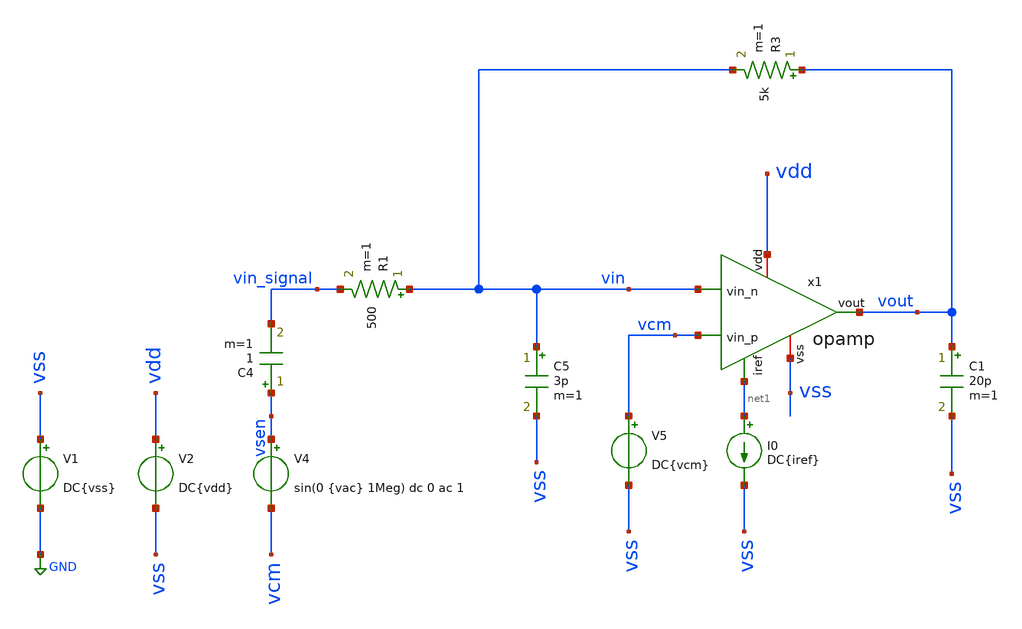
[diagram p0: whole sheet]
** sch_path: tb_opamp_closeloop.sch
**.subckt tb_opamp_closeloop
V1 vss GND DC{vss}
V2 vdd vss DC{vdd}
V4 vsen vcm sin(0 {vac} 1Meg) dc 0 ac 1
C4 vsen vin_signal 1 m=1
I0 net1 vss DC{iref}
R1 vin vin_signal 500 m=1
R3 vout vin 5k m=1
C5 vin vss 3p m=1
C1 vout vss 20p m=1
V5 vcm vss DC{vcm}
x1 vdd net1 vin vcm vout vss opamp
**** begin user architecture code




* Circuit Parameters
.param iref = 100u
.param vdd  = 1.8
.param vss  = 0.0
.param vcm  = vdd/2
.param vac  = 60m

.param mul8 = 2
.param mul5 = 20
.param mul7 = 150
.param w857 = 70
.param l857 = 7

.param l34  = 3
.param w34  = 60
.param mul34 = 2

.param mpar = 333
.param lpar = 0.5
.param wpar = 10

.param mul6 = 90
.param l6   = 0.15
.param w6   = 25

.param mul9 = 1
.param l9   = 0.15
.param w9   = 10

.param res_1 = 333
.param cap_1 = 5p

.options TEMP = 65

* Include Models
.lib ~/skywater/skywater-pdk/libraries/sky130_fd_pr_ngspice/latest/models/corners/sky130.lib TT

* OP Parameters & Singals to save
.save all  @M.X1.XM1.msky130_fd_pr__pfet_01v8_lvt[id] @M.X1.XM1.msky130_fd_pr__pfet_01v8_lvt[vth] @M.X1.XM1.msky130_fd_pr__pfet_01v8_lvt[vgs] @M.X1.XM1.msky130_fd_pr__pfet_01v8_lvt[vds] @M.X1.XM1.msky130_fd_pr__pfet_01v8_lvt[vdsat] @M.X1.XM1.msky130_fd_pr__pfet_01v8_lvt[gm] @M.X1.XM1.msky130_fd_pr__pfet_01v8_lvt[gds]  @M.X1.XM2.msky130_fd_pr__pfet_01v8_lvt[id] @M.X1.XM2.msky130_fd_pr__pfet_01v8_lvt[vth] @M.X1.XM2.msky130_fd_pr__pfet_01v8_lvt[vgs] @M.X1.XM2.msky130_fd_pr__pfet_01v8_lvt[vds] @M.X1.XM2.msky130_fd_pr__pfet_01v8_lvt[vdsat] @M.X1.XM2.msky130_fd_pr__pfet_01v8_lvt[gm] @M.X1.XM2.msky130_fd_pr__pfet_01v8_lvt[gds]  @M.X1.XM3.msky130_fd_pr__nfet_01v8[id] @M.X1.XM3.msky130_fd_pr__nfet_01v8[vth] @M.X1.XM3.msky130_fd_pr__nfet_01v8[vgs] @M.X1.XM3.msky130_fd_pr__nfet_01v8[vds] @M.X1.XM3.msky130_fd_pr__nfet_01v8[vdsat] @M.X1.XM3.msky130_fd_pr__nfet_01v8[gm] @M.X1.XM3.msky130_fd_pr__nfet_01v8[gds]  @M.X1.XM4.msky130_fd_pr__nfet_01v8[id] @M.X1.XM4.msky130_fd_pr__nfet_01v8[vth] @M.X1.XM4.msky130_fd_pr__nfet_01v8[vgs] @M.X1.XM4.msky130_fd_pr__nfet_01v8[vds] @M.X1.XM4.msky130_fd_pr__nfet_01v8[vdsat] @M.X1.XM4.msky130_fd_pr__nfet_01v8[gm] @M.X1.XM4.msky130_fd_pr__nfet_01v8[gds]  @M.X1.XM5.msky130_fd_pr__pfet_01v8[id] @M.X1.XM5.msky130_fd_pr__pfet_01v8[vth] @M.X1.XM5.msky130_fd_pr__pfet_01v8[vgs] @M.X1.XM5.msky130_fd_pr__pfet_01v8[vds] @M.X1.XM5.msky130_fd_pr__pfet_01v8[vdsat] @M.X1.XM5.msky130_fd_pr__pfet_01v8[gm] @M.X1.XM5.msky130_fd_pr__pfet_01v8[gds]  @M.X1.XM6.msky130_fd_pr__nfet_01v8[id] @M.X1.XM6.msky130_fd_pr__nfet_01v8[vth] @M.X1.XM6.msky130_fd_pr__nfet_01v8[vgs] @M.X1.XM6.msky130_fd_pr__nfet_01v8[vds] @M.X1.XM6.msky130_fd_pr__nfet_01v8[vdsat] @M.X1.XM6.msky130_fd_pr__nfet_01v8[gm] @M.X1.XM6.msky130_fd_pr__nfet_01v8[gds]  @M.X1.XM7.msky130_fd_pr__pfet_01v8[id] @M.X1.XM7.msky130_fd_pr__pfet_01v8[vth] @M.X1.XM7.msky130_fd_pr__pfet_01v8[vgs] @M.X1.XM7.msky130_fd_pr__pfet_01v8[vds] @M.X1.XM7.msky130_fd_pr__pfet_01v8[vdsat] @M.X1.XM7.msky130_fd_pr__pfet_01v8[gm] @M.X1.XM7.msky130_fd_pr__pfet_01v8[gds]  @M.X1.XM8.msky130_fd_pr__pfet_01v8[id] @M.X1.XM8.msky130_fd_pr__pfet_01v8[vth] @M.X1.XM8.msky130_fd_pr__pfet_01v8[vgs] @M.X1.XM8.msky130_fd_pr__pfet_01v8[vds] @M.X1.XM8.msky130_fd_pr__pfet_01v8[vdsat] @M.X1.XM8.msky130_fd_pr__pfet_01v8[gm] @M.X1.XM8.msky130_fd_pr__pfet_01v8[gds]  @M.X1.XM9.msky130_fd_pr__nfet_01v8[id] @M.X1.XM9.msky130_fd_pr__nfet_01v8[vth] @M.X1.XM9.msky130_fd_pr__nfet_01v8[vgs] @M.X1.XM9.msky130_fd_pr__nfet_01v8[vds] @M.X1.XM9.msky130_fd_pr__nfet_01v8[vdsat] @M.X1.XM9.msky130_fd_pr__nfet_01v8[gm] @M.X1.XM9.msky130_fd_pr__nfet_01v8[gds]  @M.X1.XM6.msky130_fd_pr__nfet_01v8[cgg] @M.X1.XM1.msky130_fd_pr__nfet_01v8[vdsat] @M.X1.XM2.msky130_fd_pr__nfet_01v8[vdsat] @M.X1.XM3.msky130_fd_pr__nfet_01v8[vdsat] @M.X1.XM4.msky130_fd_pr__nfet_01v8[vdsat] @M.X1.XM5.msky130_fd_pr__nfet_01v8[vdsat] @M.X1.XM6.msky130_fd_pr__nfet_01v8[vdsat] @M.X1.XM7.msky130_fd_pr__nfet_01v8[vdsat] @M.X1.XM8.msky130_fd_pr__nfet_01v8[vdsat] @M.X1.XM9.msky130_fd_pr__nfet_01v8[vdsat]
*
*Simulation
.control
  set color1 = purple
  set color0 = white
  ac dec 100 1k 10G
  setplot ac1
  meas ac GBW when vdb(vout)=0
  meas ac DCG find vdb(vout) at=1k
  plot vdb(vout) {vp(vout)*180/PI}

  reset
  tran 0.01u 11u
  setplot tran1
  plot v(vsen) v(vout)

  *reset
  *noise v(vout) V4 dec 100 1k 10G 1
  *setplot noise1
  *plot inoise_spectrum onoise_spectrum
  *plot onoise_spectrum onoise_spectrum
  *setplot noise2
  *print inoise_total
  *print onoise_total
  *print onoise_total.m.x1.xm1.msky130_fd_pr__pfet_01v8_lvt.1overf
  *print onoise_total.m.x1.xm1.msky130_fd_pr__pfet_01v8_lvt.id
  *print onoise_total.m.x1.xm2.msky130_fd_pr__pfet_01v8_lvt.1overf
  *print onoise_total.m.x1.xm2.msky130_fd_pr__pfet_01v8_lvt.id
  *print onoise_total.m.x1.xm3.msky130_fd_pr__nfet_01v8.1overf
  *print onoise_total.m.x1.xm3.msky130_fd_pr__nfet_01v8.id
  *print onoise_total.m.x1.xm4.msky130_fd_pr__nfet_01v8.1overf
  *print onoise_total.m.x1.xm4.msky130_fd_pr__nfet_01v8.id
  *print onoise_total.m.x1.xm5.msky130_fd_pr__pfet_01v8.1overf
  *print onoise_total.m.x1.xm5.msky130_fd_pr__pfet_01v8.id
  *print onoise_total.m.x1.xm6.msky130_fd_pr__nfet_01v8.1overf
  *print onoise_total.m.x1.xm6.msky130_fd_pr__nfet_01v8.id
  *print onoise_total.m.x1.xm7.msky130_fd_pr__pfet_01v8.1overf
  *print onoise_total.m.x1.xm7.msky130_fd_pr__pfet_01v8.id
  *print onoise_total.m.x1.xm8.msky130_fd_pr__pfet_01v8.1overf
  *print onoise_total.m.x1.xm8.msky130_fd_pr__pfet_01v8.id
  *set filetype=ascii
  *write tpfinal_noise.raw
  reset
  set sqrnoise
  noise v(vout) V4 dec 100 1k 10G 1
  setplot noise1
  plot onoise_spectrum
  plot sqrt(integ(onoise_spectrum))
  let onoise_total_integrado = maximum(sqrt(integ(onoise_spectrum)))
  print onoise_total_integrado

  reset
  tran 0.01u 11u
  fourier 1e6 vout
  let THD_db = db(fourier11[1][3]/fourier11[1][1])
  print THD_db
  fft vout
  plot mag(vout)
  plot db(mag(vout))

  reset
  op
  setplot op1
  unset filetype
  write tb_opamp_closeloop.raw
.endc

.end


**** end user architecture code
**.ends

* expanding   symbol:  opamp.sym # of pins=6
** sym_path: opamp.sym
** sch_path: opamp.sch
.subckt opamp vdd iref vin_n vin_p vout vss
*.iopin vdd
*.iopin vss
*.ipin vin_n
*.ipin vin_p
*.ipin iref
*.opin vout
XM3 vbn vbn vss vss sky130_fd_pr__nfet_01v8 L={L34} W={W34} nf=1 ad='W * 0.29' as='W * 0.29' pd='2 * (W + 0.29)'
+ ps='2 * (W + 0.29)' nrd='0.29 / W' nrs='0.29 / W' sa=0 sb=0 sd=0 mult={mul34} m={mul34}
XM4 voe1 vbn vss vss sky130_fd_pr__nfet_01v8 L={L34} W={W34} nf=1 ad='W * 0.29' as='W * 0.29' pd='2 * (W + 0.29)'
+ ps='2 * (W + 0.29)' nrd='0.29 / W' nrs='0.29 / W' sa=0 sb=0 sd=0 mult={mul34} m={mul34}
XM5 vp iref vdd vdd sky130_fd_pr__pfet_01v8 L={L857} W={W857} nf=1 ad='W * 0.29' as='W * 0.29' pd='2 * (W + 0.29)'
+ ps='2 * (W + 0.29)' nrd='0.29 / W' nrs='0.29 / W' sa=0 sb=0 sd=0 mult={mul5} m={mul5}
XM7 vout iref vdd vdd sky130_fd_pr__pfet_01v8 L={L857} W={W857} nf=1 ad='W * 0.29' as='W * 0.29' pd='2 * (W + 0.29)'
+ ps='2 * (W + 0.29)' nrd='0.29 / W' nrs='0.29 / W' sa=0 sb=0 sd=0 mult={mul7} m={mul7}
XM8 iref iref vdd vdd sky130_fd_pr__pfet_01v8 L={L857} W={W857} nf=1 ad='W * 0.29' as='W * 0.29' pd='2 * (W + 0.29)'
+ ps='2 * (W + 0.29)' nrd='0.29 / W' nrs='0.29 / W' sa=0 sb=0 sd=0 mult={mul8} m={mul8}
XM9 net1 vdd voe1 vss sky130_fd_pr__nfet_01v8 L={l9} W={w9} nf=1 ad='W * 0.29' as='W * 0.29' pd='2 * (W + 0.29)'
+ ps='2 * (W + 0.29)' nrd='0.29 / W' nrs='0.29 / W' sa=0 sb=0 sd=0 mult={mul9} m={mul9}
XM6 vout voe1 vss vss sky130_fd_pr__nfet_01v8 L={l6} W={w6} nf=1 ad='W * 0.29' as='W * 0.29' pd='2 * (W + 0.29)'
+ ps='2 * (W + 0.29)' nrd='0.29 / W' nrs='0.29 / W' sa=0 sb=0 sd=0 mult={mul6} m={mul6}
XM1 vbn vin_n vp vp sky130_fd_pr__pfet_01v8_lvt L={lpar} W={wpar} nf=1 ad='int((nf+1)/2) * W/nf * 0.29'
+ as='int((nf+2)/2) * W/nf * 0.29' pd='2*int((nf+1)/2) * (W/nf + 0.29)' ps='2*int((nf+2)/2) * (W/nf + 0.29)'
+ nrd='0.29 / W' nrs='0.29 / W' sa=0 sb=0 sd=0 mult={mpar} m={mpar}
XM2 voe1 vin_p vp vp sky130_fd_pr__pfet_01v8_lvt L={lpar} W={wpar} nf=1 ad='int((nf+1)/2) * W/nf * 0.29'
+ as='int((nf+2)/2) * W/nf * 0.29' pd='2*int((nf+1)/2) * (W/nf + 0.29)' ps='2*int((nf+2)/2) * (W/nf + 0.29)'
+ nrd='0.29 / W' nrs='0.29 / W' sa=0 sb=0 sd=0 mult={mpar} m={mpar}
C1 net1 vout {cap_1} m=1
R1 vdd vdd {res_1} m=1
.ends

.GLOBAL GND
.end
